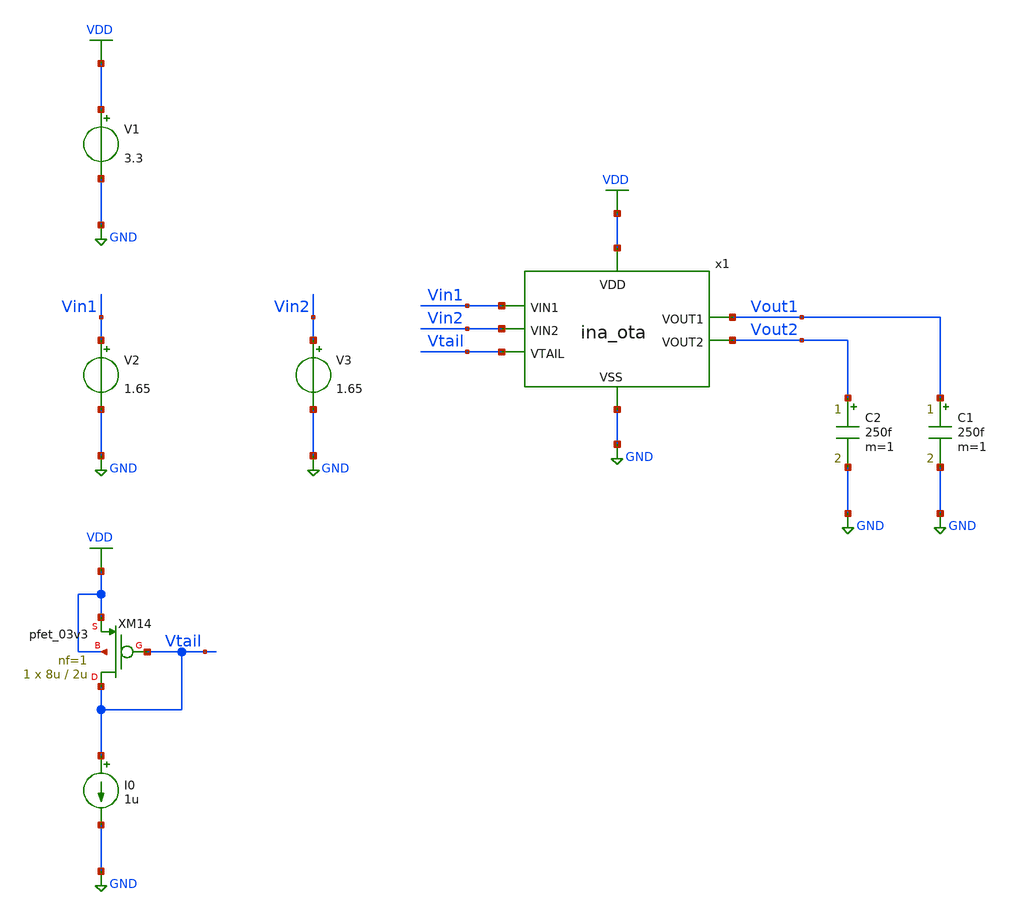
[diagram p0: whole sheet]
** sch_path: designs/libs/tb_ina/tb_ina_ota_op/tb_ina_ota_op.sch
**.subckt tb_ina_ota_op
V1 VDD GND 3.3
V2 Vin1 GND 1.65
V3 Vin2 GND 1.65
C2 Vout2 GND 250f m=1
C1 Vout1 GND 250f m=1
XM14 Vtail Vtail VDD VDD pfet_03v3 L=2u W=8u nf=1 ad='int((nf+1)/2) * W/nf * 0.18u' as='int((nf+2)/2) * W/nf * 0.18u'
+ pd='2*int((nf+1)/2) * (W/nf + 0.18u)' ps='2*int((nf+2)/2) * (W/nf + 0.18u)' nrd='0.18u / W' nrs='0.18u / W'
+ sa=0 sb=0 sd=0 m=1
I0 Vtail GND 1u
x1 VDD Vtail Vin1 Vout2 Vout1 Vin2 GND ina_ota
**** begin user architecture code

.include $::180MCU_MODELS/design.ngspice
.lib $::180MCU_MODELS/sm141064.ngspice typical
.lib $::180MCU_MODELS/sm141064.ngspice cap_mim
.lib $::180MCU_MODELS/sm141064.ngspice moscap_typical
.lib $::180MCU_MODELS/sm141064.ngspice mimcap_typical
.lib $::180MCU_MODELS/sm141064.ngspice res_typical
* .lib $::180MCU_MODELS/sm141064.ngspice res_statistical
* ngspice commands




.control
save all

set color0 = white

*************************************
** PARAMETERS
*************************************

let Vdd   = 3.3
let Vcm   = 1.65
let Ibias = 2u

*************************************
** SOURCES
*************************************

alter @V1[DC] = $&Vdd
alter @V2[DC] = $&Vcm
alter @V3[DC] = $&Vcm
alter @I0[DC] = $&Ibias

*************************************
** OPERATING POINT SIMULATION
*************************************

op

*************************************
** PRINT RESULTS
*************************************

echo ------ PMOS ---------
echo ------ XM1 ----------
let XM1_vgs = @m.x1.xm1.m0[vgs]
let XM1_vds = @m.x1.xm1.m0[vds]
let XM1_id = @m.x1.xm1.m0[id]
let XM1_gm = @m.x1.xm1.m0[gm]
let XM1_gds = @m.x1.xm1.m0[gds]
let XM1_cgg = @m.x1.xm1.m0[cgg]
let XM1_gm_id = XM1_gm/abs(XM1_id)
print XM1_vgs
print XM1_vds
print XM1_id
print XM1_gm
print XM1_gds
print XM1_cgg
print XM1_gm_id
echo ------ XM2 ----------
let XM2_vgs = @m.x1.xm2.m0[vgs]
let XM2_vds = @m.x1.xm2.m0[vds]
let XM2_id = @m.x1.xm2.m0[id]
let XM2_gm = @m.x1.xm2.m0[gm]
let XM2_gds = @m.x1.xm2.m0[gds]
let XM2_cgg = @m.x1.xm2.m0[cgg]
let XM2_gm_id = XM2_gm/abs(XM2_id)
print XM2_vgs
print XM2_vds
print XM2_id
print XM2_gm
print XM2_gds
print XM2_cgg
print XM2_gm_id
echo ------ XM3 ----------
let XM3_vgs = @m.x1.xm3.m0[vgs]
let XM3_vds = @m.x1.xm3.m0[vds]
let XM3_id = @m.x1.xm3.m0[id]
let XM3_gm = @m.x1.xm3.m0[gm]
let XM3_gds = @m.x1.xm3.m0[gds]
let XM3_cgg = @m.x1.xm3.m0[cgg]
let XM3_gm_id = XM3_gm/abs(XM3_id)
print XM3_vgs
print XM3_vds
print XM3_id
print XM3_gm
print XM3_gds
print XM3_cgg
print XM3_gm_id
echo ------ XM4 ----------
let XM4_vgs = @m.x1.xm4.m0[vgs]
let XM4_vds = @m.x1.xm4.m0[vds]
let XM4_id = @m.x1.xm4.m0[id]
let XM4_gm = @m.x1.xm4.m0[gm]
let XM4_gds = @m.x1.xm4.m0[gds]
let XM4_cgg = @m.x1.xm4.m0[cgg]
let XM4_gm_id = XM4_gm/abs(XM4_id)
print XM4_vgs
print XM4_vds
print XM4_id
print XM4_gm
print XM4_gds
print XM4_cgg
print XM4_gm_id
echo ------ XM5 ----------
let XM5_vgs = @m.x1.xm5.m0[vgs]
let XM5_vds = @m.x1.xm5.m0[vds]
let XM5_id = @m.x1.xm5.m0[id]
let XM5_gm = @m.x1.xm5.m0[gm]
let XM5_gds = @m.x1.xm5.m0[gds]
let XM5_cgg = @m.x1.xm5.m0[cgg]
let XM5_gm_id = XM5_gm/abs(XM5_id)
print XM5_vgs
print XM5_vds
print XM5_id
print XM5_gm
print XM5_gds
print XM5_cgg
print XM5_gm_id
echo ------ XM10 ----------
let XM10_vgs = @m.x1.xm10.m0[vgs]
let XM10_vds = @m.x1.xm10.m0[vds]
let XM10_id = @m.x1.xm10.m0[id]
let XM10_gm = @m.x1.xm10.m0[gm]
let XM10_gds = @m.x1.xm10.m0[gds]
let XM10_cgg = @m.x1.xm10.m0[cgg]
let XM10_gm_id = XM10_gm/abs(XM10_id)
print XM10_vgs
print XM10_vds
print XM10_id
print XM10_gm
print XM10_gds
print XM10_cgg
print XM10_gm_id
echo ------ XM13 ----------
let XM13_vgs = @m.x1.xm13.m0[vgs]
let XM13_vds = @m.x1.xm13.m0[vds]
let XM13_id = @m.x1.xm13.m0[id]
let XM13_gm = @m.x1.xm13.m0[gm]
let XM13_gds = @m.x1.xm13.m0[gds]
let XM13_cgg = @m.x1.xm13.m0[cgg]
let XM13_gm_id = XM13_gm/abs(XM13_id)
print XM13_vgs
print XM13_vds
print XM13_id
print XM13_gm
print XM13_gds
print XM13_cgg
print XM13_gm_id

echo ------ NMOS ---------
echo ------ XM6 ----------
let XM6_vgs = @m.x1.xm6.m0[vgs]
let XM6_vds = @m.x1.xm6.m0[vds]
let XM6_id = @m.x1.xm6.m0[id]
let XM6_gm = @m.x1.xm6.m0[gm]
let XM6_gds = @m.x1.xm6.m0[gds]
let XM6_cgg = @m.x1.xm6.m0[cgg]
let XM6_gm_id = XM6_gm/abs(XM6_id)
print XM6_vgs
print XM6_vds
print XM6_id
print XM6_gm
print XM6_gds
print XM6_cgg
print XM6_gm_id
echo ------ XM7 ----------
let XM7_vgs = @m.x1.xm7.m0[vgs]
let XM7_vds = @m.x1.xm7.m0[vds]
let XM7_id = @m.x1.xm7.m0[id]
let XM7_gm = @m.x1.xm7.m0[gm]
let XM7_gds = @m.x1.xm7.m0[gds]
let XM7_cgg = @m.x1.xm7.m0[cgg]
let XM7_gm_id = XM7_gm/abs(XM7_id)
print XM7_vgs
print XM7_vds
print XM7_id
print XM7_gm
print XM7_gds
print XM7_cgg
print XM7_gm_id
echo ------ XM8 ----------
let XM8_vgs = @m.x1.xm8.m0[vgs]
let XM8_vds = @m.x1.xm8.m0[vds]
let XM8_id = @m.x1.xm8.m0[id]
let XM8_gm = @m.x1.xm8.m0[gm]
let XM8_gds = @m.x1.xm8.m0[gds]
let XM8_cgg = @m.x1.xm8.m0[cgg]
let XM8_gm_id = XM8_gm/abs(XM8_id)
print XM8_vgs
print XM8_vds
print XM8_id
print XM8_gm
print XM8_gds
print XM8_cgg
print XM8_gm_id
echo ------ XM9 ----------
let XM9_vgs = @m.x1.xm9.m0[vgs]
let XM9_vds = @m.x1.xm9.m0[vds]
let XM9_id = @m.x1.xm9.m0[id]
let XM9_gm = @m.x1.xm9.m0[gm]
let XM9_gds = @m.x1.xm9.m0[gds]
let XM9_cgg = @m.x1.xm9.m0[cgg]
let XM9_gm_id = XM9_gm/abs(XM9_id)
print XM9_vgs
print XM9_vds
print XM9_id
print XM9_gm
print XM9_gds
print XM9_cgg
print XM9_gm_id
echo ------ XM11 ----------
let XM11_vgs = @m.x1.xm11.m0[vgs]
let XM11_vds = @m.x1.xm11.m0[vds]
let XM11_id = @m.x1.xm11.m0[id]
let XM11_gm = @m.x1.xm11.m0[gm]
let XM11_gds = @m.x1.xm11.m0[gds]
let XM11_cgg = @m.x1.xm11.m0[cgg]
let XM11_gm_id = XM11_gm/abs(XM11_id)
print XM11_vgs
print XM11_vds
print XM11_id
print XM11_gm
print XM11_gds
print XM11_cgg
print XM11_gm_id
echo ------ XM12 ----------
let XM12_vgs = @m.x1.xm12.m0[vgs]
let XM12_vds = @m.x1.xm12.m0[vds]
let XM12_id = @m.x1.xm12.m0[id]
let XM12_gm = @m.x1.xm12.m0[gm]
let XM12_gds = @m.x1.xm12.m0[gds]
let XM12_cgg = @m.x1.xm12.m0[cgg]
let XM12_gm_id = XM12_gm/abs(XM12_id)
print XM12_vgs
print XM12_vds
print XM12_id
print XM12_gm
print XM12_gds
print XM12_cgg
print XM12_gm_id

echo ------ OTA -----------
let Iota = -i(v1) - 1u
let Pota = Vdd*Iota
print Iota
print Pota

*************************************
** SAVE
*************************************

write tb_ina_ota_op.raw

.endc
* ngspice commands



**** end user architecture code
**.ends

* expanding   symbol:  libs/core_ina/ina_ota/ina_ota.sym # of pins=7
** sym_path: designs/libs/core_ina/ina_ota/ina_ota.sym
** sch_path: designs/libs/core_ina/ina_ota/ina_ota.sch
.subckt ina_ota VDD VTAIL VIN1 VOUT2 VOUT1 VIN2 VSS
*.ipin Vin1
*.ipin Vin2
*.ipin Vtail
*.ipin VSS
*.opin Vout1
*.ipin VDD
*.opin Vout2
XM2 net4 net4 VDD VDD pfet_03v3 L=6u W=0.65u nf=1 ad='int((nf+1)/2) * W/nf * 0.18u' as='int((nf+2)/2) * W/nf * 0.18u'
+ pd='2*int((nf+1)/2) * (W/nf + 0.18u)' ps='2*int((nf+2)/2) * (W/nf + 0.18u)' nrd='0.18u / W' nrs='0.18u / W'
+ sa=0 sb=0 sd=0 m=1
XM1 net3 Vtail VDD VDD pfet_03v3 L=2u W=8u nf=1 ad='int((nf+1)/2) * W/nf * 0.18u' as='int((nf+2)/2) * W/nf * 0.18u'
+ pd='2*int((nf+1)/2) * (W/nf + 0.18u)' ps='2*int((nf+2)/2) * (W/nf + 0.18u)' nrd='0.18u / W' nrs='0.18u / W'
+ sa=0 sb=0 sd=0 m=1
XM3 net5 net5 VDD VDD pfet_03v3 L=6u W=0.65u nf=1 ad='int((nf+1)/2) * W/nf * 0.18u' as='int((nf+2)/2) * W/nf * 0.18u'
+ pd='2*int((nf+1)/2) * (W/nf + 0.18u)' ps='2*int((nf+2)/2) * (W/nf + 0.18u)' nrd='0.18u / W' nrs='0.18u / W'
+ sa=0 sb=0 sd=0 m=1
XM4 net1 Vin1 net3 VDD pfet_03v3 L=0.28u W=15u nf=1 ad='int((nf+1)/2) * W/nf * 0.18u' as='int((nf+2)/2) * W/nf * 0.18u'
+ pd='2*int((nf+1)/2) * (W/nf + 0.18u)' ps='2*int((nf+2)/2) * (W/nf + 0.18u)' nrd='0.18u / W' nrs='0.18u / W'
+ sa=0 sb=0 sd=0 m=10
XM5 net2 Vin2 net3 VDD pfet_03v3 L=0.28u W=15u nf=1 ad='int((nf+1)/2) * W/nf * 0.18u' as='int((nf+2)/2) * W/nf * 0.18u'
+ pd='2*int((nf+1)/2) * (W/nf + 0.18u)' ps='2*int((nf+2)/2) * (W/nf + 0.18u)' nrd='0.18u / W' nrs='0.18u / W'
+ sa=0 sb=0 sd=0 m=10
XM6 net4 net1 VSS VSS nfet_03v3 L=6u W=1.8u nf=1 ad='int((nf+1)/2) * W/nf * 0.18u' as='int((nf+2)/2) * W/nf * 0.18u'
+ pd='2*int((nf+1)/2) * (W/nf + 0.18u)' ps='2*int((nf+2)/2) * (W/nf + 0.18u)' nrd='0.18u / W' nrs='0.18u / W'
+ sa=0 sb=0 sd=0 m=1
XM7 net5 net2 VSS VSS nfet_03v3 L=6u W=1.8u nf=1 ad='int((nf+1)/2) * W/nf * 0.18u' as='int((nf+2)/2) * W/nf * 0.18u'
+ pd='2*int((nf+1)/2) * (W/nf + 0.18u)' ps='2*int((nf+2)/2) * (W/nf + 0.18u)' nrd='0.18u / W' nrs='0.18u / W'
+ sa=0 sb=0 sd=0 m=1
XM8 net1 net1 VSS VSS nfet_03v3 L=6u W=1.8u nf=1 ad='int((nf+1)/2) * W/nf * 0.18u' as='int((nf+2)/2) * W/nf * 0.18u'
+ pd='2*int((nf+1)/2) * (W/nf + 0.18u)' ps='2*int((nf+2)/2) * (W/nf + 0.18u)' nrd='0.18u / W' nrs='0.18u / W'
+ sa=0 sb=0 sd=0 m=1
XM9 net2 net2 VSS VSS nfet_03v3 L=6u W=1.8u nf=1 ad='int((nf+1)/2) * W/nf * 0.18u' as='int((nf+2)/2) * W/nf * 0.18u'
+ pd='2*int((nf+1)/2) * (W/nf + 0.18u)' ps='2*int((nf+2)/2) * (W/nf + 0.18u)' nrd='0.18u / W' nrs='0.18u / W'
+ sa=0 sb=0 sd=0 m=1
XM10 Vout1 net4 VDD VDD pfet_03v3 L=6u W=0.65u nf=1 ad='int((nf+1)/2) * W/nf * 0.18u' as='int((nf+2)/2) * W/nf * 0.18u'
+ pd='2*int((nf+1)/2) * (W/nf + 0.18u)' ps='2*int((nf+2)/2) * (W/nf + 0.18u)' nrd='0.18u / W' nrs='0.18u / W'
+ sa=0 sb=0 sd=0 m=1
XM11 Vout1 net2 VSS VSS nfet_03v3 L=6u W=1.8u nf=1 ad='int((nf+1)/2) * W/nf * 0.18u' as='int((nf+2)/2) * W/nf * 0.18u'
+ pd='2*int((nf+1)/2) * (W/nf + 0.18u)' ps='2*int((nf+2)/2) * (W/nf + 0.18u)' nrd='0.18u / W' nrs='0.18u / W'
+ sa=0 sb=0 sd=0 m=1
XM12 Vout2 net1 VSS VSS nfet_03v3 L=6u W=1.8u nf=1 ad='int((nf+1)/2) * W/nf * 0.18u' as='int((nf+2)/2) * W/nf * 0.18u'
+ pd='2*int((nf+1)/2) * (W/nf + 0.18u)' ps='2*int((nf+2)/2) * (W/nf + 0.18u)' nrd='0.18u / W' nrs='0.18u / W'
+ sa=0 sb=0 sd=0 m=1
XM13 Vout2 net5 VDD VDD pfet_03v3 L=6u W=0.65u nf=1 ad='int((nf+1)/2) * W/nf * 0.18u' as='int((nf+2)/2) * W/nf * 0.18u'
+ pd='2*int((nf+1)/2) * (W/nf + 0.18u)' ps='2*int((nf+2)/2) * (W/nf + 0.18u)' nrd='0.18u / W' nrs='0.18u / W'
+ sa=0 sb=0 sd=0 m=1
.ends

.GLOBAL GND
.GLOBAL VDD
.end
